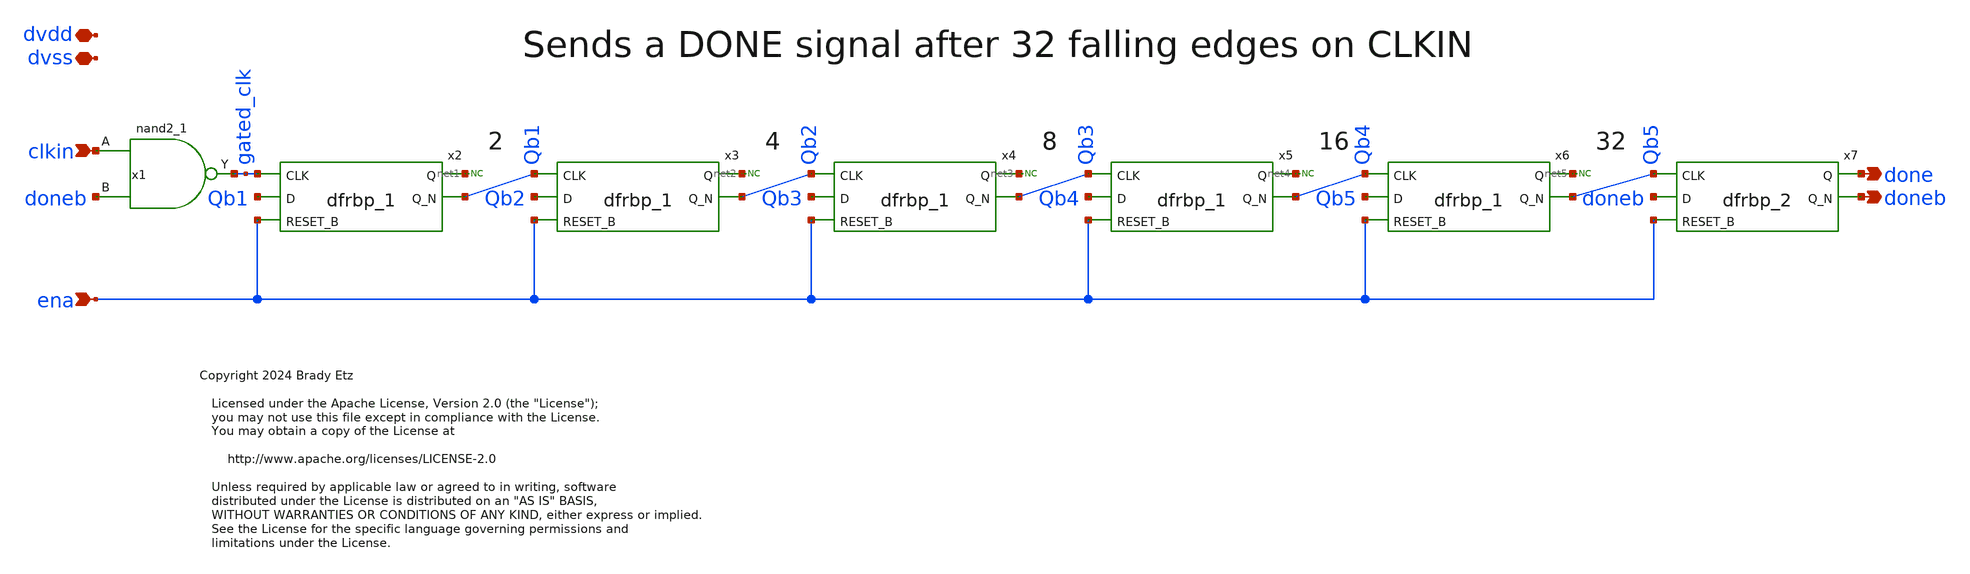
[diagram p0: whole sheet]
** sch_path: xschem/ena_rip_dly.sch
* Copyright 2024 Brady Etz
* Licensed under the Apache License, Version 2.0 (the "License");
**.subckt ena_rip_dly clkin ena done doneb dvdd dvss
*.ipin clkin
*.ipin ena
*.opin done
*.opin doneb
*.iopin dvdd
*.iopin dvss
x2 gated_clk Qb1 ena dvss dvss dvdd dvdd net1 Qb1 sky130_fd_sc_hd__dfrbp_1
x3 Qb1 Qb2 ena dvss dvss dvdd dvdd net2 Qb2 sky130_fd_sc_hd__dfrbp_1
x4 Qb2 Qb3 ena dvss dvss dvdd dvdd net3 Qb3 sky130_fd_sc_hd__dfrbp_1
x5 Qb3 Qb4 ena dvss dvss dvdd dvdd net4 Qb4 sky130_fd_sc_hd__dfrbp_1
x6 Qb4 Qb5 ena dvss dvss dvdd dvdd net5 Qb5 sky130_fd_sc_hd__dfrbp_1
x1 clkin doneb dvss dvss dvdd dvdd gated_clk sky130_fd_sc_hd__nand2_1
* noconn #net1
* noconn #net2
* noconn #net3
* noconn #net4
* noconn #net5
x7 Qb5 doneb ena dvss dvss dvdd dvdd done doneb sky130_fd_sc_hd__dfrbp_2
**.ends
.end
